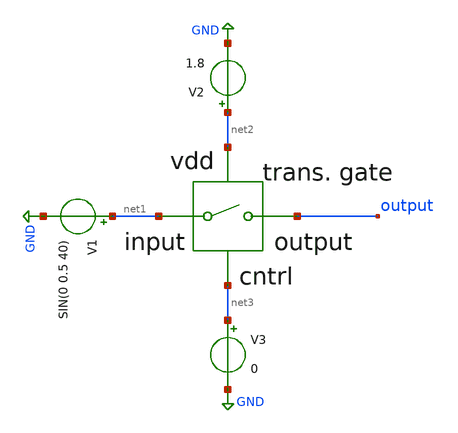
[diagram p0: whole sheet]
** sch_path: xschem/attenuator/trans-gate-testbench.sch
**.subckt trans-gate-testbench
V1 net1 GND SIN(0 0.5 40)
V2 net2 GND 1.8
V3 net3 GND 0
**** begin user architecture code
 ** manual skywater pdks install (with patches applied)
* .lib $::SKYWATER_MODELS/models/sky130.lib.spice tt

** opencircuitdesign pdks install
.lib $::SKYWATER_MODELS/sky130.lib.spice tt

.param mc_mm_switch=0
.param mc_pr_switch=0



.tran 0.001s 0.1s
.control
  run
  plot v(output) v(net1)
.endc
.save all


**** end user architecture code
**.ends
.GLOBAL GND
.end
